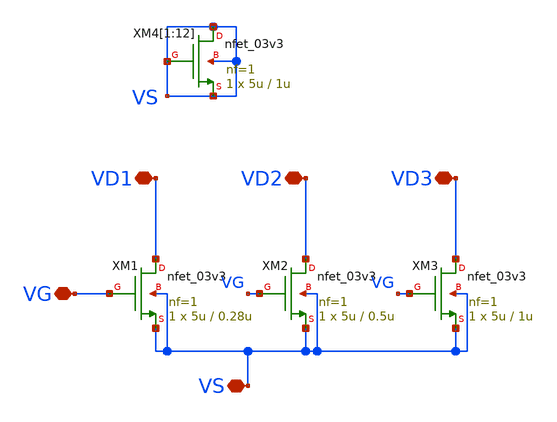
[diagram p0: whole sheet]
** sch_path: Current_Source/nmos_char.sch
**.subckt nmos_char VD1 VD2 VD3 VG VS
*.iopin VD1
*.iopin VD2
*.iopin VD3
*.iopin VG
*.iopin VS
XM1 VD1 VG VS VS nfet_03v3 L=0.28u W=5u nf=1 ad='int((nf+1)/2) * W/nf * 0.18u' as='int((nf+2)/2) * W/nf * 0.18u'
+ pd='2*int((nf+1)/2) * (W/nf + 0.18u)' ps='2*int((nf+2)/2) * (W/nf + 0.18u)' nrd='0.18u / W' nrs='0.18u / W'
+ sa=0 sb=0 sd=0 m=1
XM2 VD2 VG VS VS nfet_03v3 L=0.5u W=5u nf=1 ad='int((nf+1)/2) * W/nf * 0.18u' as='int((nf+2)/2) * W/nf * 0.18u'
+ pd='2*int((nf+1)/2) * (W/nf + 0.18u)' ps='2*int((nf+2)/2) * (W/nf + 0.18u)' nrd='0.18u / W' nrs='0.18u / W'
+ sa=0 sb=0 sd=0 m=1
XM3 VD3 VG VS VS nfet_03v3 L=1u W=5u nf=1 ad='int((nf+1)/2) * W/nf * 0.18u' as='int((nf+2)/2) * W/nf * 0.18u'
+ pd='2*int((nf+1)/2) * (W/nf + 0.18u)' ps='2*int((nf+2)/2) * (W/nf + 0.18u)' nrd='0.18u / W' nrs='0.18u / W'
+ sa=0 sb=0 sd=0 m=1
XM4[1] VS VS VS VS nfet_03v3 L=1u W=5u nf=1 ad='int((nf+1)/2) * W/nf * 0.18u' as='int((nf+2)/2) * W/nf * 0.18u'
+ pd='2*int((nf+1)/2) * (W/nf + 0.18u)' ps='2*int((nf+2)/2) * (W/nf + 0.18u)' nrd='0.18u / W' nrs='0.18u / W'
+ sa=0 sb=0 sd=0 m=1
XM4[2] VS VS VS VS nfet_03v3 L=1u W=5u nf=1 ad='int((nf+1)/2) * W/nf * 0.18u' as='int((nf+2)/2) * W/nf * 0.18u'
+ pd='2*int((nf+1)/2) * (W/nf + 0.18u)' ps='2*int((nf+2)/2) * (W/nf + 0.18u)' nrd='0.18u / W' nrs='0.18u / W'
+ sa=0 sb=0 sd=0 m=1
XM4[3] VS VS VS VS nfet_03v3 L=1u W=5u nf=1 ad='int((nf+1)/2) * W/nf * 0.18u' as='int((nf+2)/2) * W/nf * 0.18u'
+ pd='2*int((nf+1)/2) * (W/nf + 0.18u)' ps='2*int((nf+2)/2) * (W/nf + 0.18u)' nrd='0.18u / W' nrs='0.18u / W'
+ sa=0 sb=0 sd=0 m=1
XM4[4] VS VS VS VS nfet_03v3 L=1u W=5u nf=1 ad='int((nf+1)/2) * W/nf * 0.18u' as='int((nf+2)/2) * W/nf * 0.18u'
+ pd='2*int((nf+1)/2) * (W/nf + 0.18u)' ps='2*int((nf+2)/2) * (W/nf + 0.18u)' nrd='0.18u / W' nrs='0.18u / W'
+ sa=0 sb=0 sd=0 m=1
XM4[5] VS VS VS VS nfet_03v3 L=1u W=5u nf=1 ad='int((nf+1)/2) * W/nf * 0.18u' as='int((nf+2)/2) * W/nf * 0.18u'
+ pd='2*int((nf+1)/2) * (W/nf + 0.18u)' ps='2*int((nf+2)/2) * (W/nf + 0.18u)' nrd='0.18u / W' nrs='0.18u / W'
+ sa=0 sb=0 sd=0 m=1
XM4[6] VS VS VS VS nfet_03v3 L=1u W=5u nf=1 ad='int((nf+1)/2) * W/nf * 0.18u' as='int((nf+2)/2) * W/nf * 0.18u'
+ pd='2*int((nf+1)/2) * (W/nf + 0.18u)' ps='2*int((nf+2)/2) * (W/nf + 0.18u)' nrd='0.18u / W' nrs='0.18u / W'
+ sa=0 sb=0 sd=0 m=1
XM4[7] VS VS VS VS nfet_03v3 L=1u W=5u nf=1 ad='int((nf+1)/2) * W/nf * 0.18u' as='int((nf+2)/2) * W/nf * 0.18u'
+ pd='2*int((nf+1)/2) * (W/nf + 0.18u)' ps='2*int((nf+2)/2) * (W/nf + 0.18u)' nrd='0.18u / W' nrs='0.18u / W'
+ sa=0 sb=0 sd=0 m=1
XM4[8] VS VS VS VS nfet_03v3 L=1u W=5u nf=1 ad='int((nf+1)/2) * W/nf * 0.18u' as='int((nf+2)/2) * W/nf * 0.18u'
+ pd='2*int((nf+1)/2) * (W/nf + 0.18u)' ps='2*int((nf+2)/2) * (W/nf + 0.18u)' nrd='0.18u / W' nrs='0.18u / W'
+ sa=0 sb=0 sd=0 m=1
XM4[9] VS VS VS VS nfet_03v3 L=1u W=5u nf=1 ad='int((nf+1)/2) * W/nf * 0.18u' as='int((nf+2)/2) * W/nf * 0.18u'
+ pd='2*int((nf+1)/2) * (W/nf + 0.18u)' ps='2*int((nf+2)/2) * (W/nf + 0.18u)' nrd='0.18u / W' nrs='0.18u / W'
+ sa=0 sb=0 sd=0 m=1
XM4[10] VS VS VS VS nfet_03v3 L=1u W=5u nf=1 ad='int((nf+1)/2) * W/nf * 0.18u' as='int((nf+2)/2) * W/nf * 0.18u'
+ pd='2*int((nf+1)/2) * (W/nf + 0.18u)' ps='2*int((nf+2)/2) * (W/nf + 0.18u)' nrd='0.18u / W' nrs='0.18u / W'
+ sa=0 sb=0 sd=0 m=1
XM4[11] VS VS VS VS nfet_03v3 L=1u W=5u nf=1 ad='int((nf+1)/2) * W/nf * 0.18u' as='int((nf+2)/2) * W/nf * 0.18u'
+ pd='2*int((nf+1)/2) * (W/nf + 0.18u)' ps='2*int((nf+2)/2) * (W/nf + 0.18u)' nrd='0.18u / W' nrs='0.18u / W'
+ sa=0 sb=0 sd=0 m=1
XM4[12] VS VS VS VS nfet_03v3 L=1u W=5u nf=1 ad='int((nf+1)/2) * W/nf * 0.18u' as='int((nf+2)/2) * W/nf * 0.18u'
+ pd='2*int((nf+1)/2) * (W/nf + 0.18u)' ps='2*int((nf+2)/2) * (W/nf + 0.18u)' nrd='0.18u / W' nrs='0.18u / W'
+ sa=0 sb=0 sd=0 m=1
**.ends
.end
